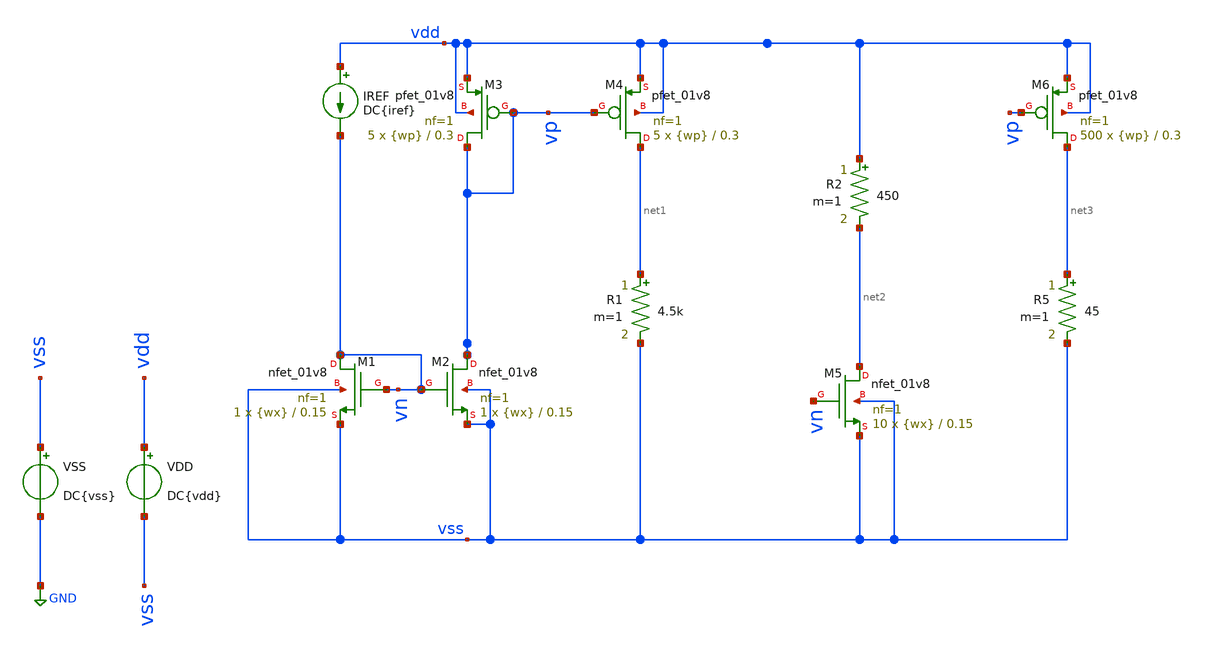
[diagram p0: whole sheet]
** sch_path: tp2/tp2_4.sch
**.subckt tp2_4
XM1 vn vn vss vss sky130_fd_pr__nfet_01v8 L=0.15 W={wx} nf=1 ad='int((nf+1)/2) * W/nf * 0.29' as='int((nf+2)/2) * W/nf * 0.29'
+ pd='2*int((nf+1)/2) * (W/nf + 0.29)' ps='2*int((nf+2)/2) * (W/nf + 0.29)' nrd='0.29 / W' nrs='0.29 / W'
+ sa=0 sb=0 sd=0 mult=1 m=1
IREF vdd vn DC{iref}
VSS vss GND DC{vss}
VDD vdd vss DC{vdd}
XM2 vp vn vss vss sky130_fd_pr__nfet_01v8 L=0.15 W={wx} nf=1 ad='int((nf+1)/2) * W/nf * 0.29' as='int((nf+2)/2) * W/nf * 0.29'
+ pd='2*int((nf+1)/2) * (W/nf + 0.29)' ps='2*int((nf+2)/2) * (W/nf + 0.29)' nrd='0.29 / W' nrs='0.29 / W'
+ sa=0 sb=0 sd=0 mult=1 m=1
XM3 vp vp vdd vdd sky130_fd_pr__pfet_01v8 L=0.3 W={wp} nf=1 ad='int((nf+1)/2) * W/nf * 0.29' as='int((nf+2)/2) * W/nf * 0.29'
+ pd='2*int((nf+1)/2) * (W/nf + 0.29)' ps='2*int((nf+2)/2) * (W/nf + 0.29)' nrd='0.29 / W' nrs='0.29 / W'
+ sa=0 sb=0 sd=0 mult=5 m=5
XM4 net1 vp vdd vdd sky130_fd_pr__pfet_01v8 L=0.3 W={wp} nf=1 ad='int((nf+1)/2) * W/nf * 0.29' as='int((nf+2)/2) * W/nf * 0.29'
+ pd='2*int((nf+1)/2) * (W/nf + 0.29)' ps='2*int((nf+2)/2) * (W/nf + 0.29)' nrd='0.29 / W' nrs='0.29 / W'
+ sa=0 sb=0 sd=0 mult=5 m=5
R1 net1 vss 4.5k m=1
XM5 net2 vn vss vss sky130_fd_pr__nfet_01v8 L=0.15 W={wx} nf=1 ad='int((nf+1)/2) * W/nf * 0.29' as='int((nf+2)/2) * W/nf * 0.29'
+ pd='2*int((nf+1)/2) * (W/nf + 0.29)' ps='2*int((nf+2)/2) * (W/nf + 0.29)' nrd='0.29 / W' nrs='0.29 / W'
+ sa=0 sb=0 sd=0 mult=10 m=10
R2 vdd net2 450 m=1
XM6 net3 vp vdd vdd sky130_fd_pr__pfet_01v8 L=0.3 W={wp} nf=1 ad='int((nf+1)/2) * W/nf * 0.29' as='int((nf+2)/2) * W/nf * 0.29'
+ pd='2*int((nf+1)/2) * (W/nf + 0.29)' ps='2*int((nf+2)/2) * (W/nf + 0.29)' nrd='0.29 / W' nrs='0.29 / W'
+ sa=0 sb=0 sd=0 mult=500 m=500
R5 net3 vss 45 m=1
**** begin user architecture code



* Parameters
.param vdd = 1.98
.param vss = 0.0
.param iref = 200u
.param wp = 97
.param wx = 2.71
.options TEMPS = 27.0

* Models
*.lib ~/skywater/skywater-pdk/libraries/sky130_fd_pr_ngspice/latest/models/corners/sky130.lib TT
.lib /foss/pdks/sky130A/libs.tech/ngspice/sky130.lib.spice tt
* Data to save
.save all  @M.XM1.msky130_fd_pr__nfet_01v8[id]  @M.XM1.msky130_fd_pr__nfet_01v8[gm]  @M.XM1.msky130_fd_pr__nfet_01v8[vds]  @M.XM1.msky130_fd_pr__nfet_01v8[vgs]  @M.XM1.msky130_fd_pr__nfet_01v8[w]  @M.XM1.msky130_fd_pr__nfet_01v8[vth]  @M.XM2.msky130_fd_pr__nfet_01v8[id]  @M.XM2.msky130_fd_pr__nfet_01v8[gm]  @M.XM2.msky130_fd_pr__nfet_01v8[vds]  @M.XM2.msky130_fd_pr__nfet_01v8[vgs]  @M.XM2.msky130_fd_pr__nfet_01v8[w]  @M.XM2.msky130_fd_pr__nfet_01v8[vth]  @M.XM2.msky130_fd_pr__nfet_01v8[vdsat]  @M.XM4.msky130_fd_pr__nfet_01v8[vdsat]  @M.XM7.msky130_fd_pr__nfet_01v8[vdsat]  @M.XM6.msky130_fd_pr__nfet_01v8[vdsat]  @M.XM5.msky130_fd_pr__nfet_01v8[vth]  @M.XM4.msky130_fd_pr__nfet_01v8[vth]  @M.XM1.msky130_fd_pr__nfet_01v8[vth]  @M.XM3.msky130_fd_pr__nfet_01v8[vth]  @M.XM7.msky130_fd_pr__nfet_01v8[vth]  @M.XM6.msky130_fd_pr__nfet_01v8[vth]  @M.XM1.msky130_fd_pr__nfet_01v8[id]  @M.XM2.msky130_fd_pr__nfet_01v8[id]  @M.XM3.msky130_fd_pr__pfet_01v8[id]  @M.XM4.msky130_fd_pr__pfet_01v8[id]  @M.XM5.msky130_fd_pr__nfet_01v8[id]  @M.XM6.msky130_fd_pr__pfet_01v8[id]

* Simulation
.control

  op
  save all
  unset filetype
  write tp2_4.raw

.endc

.end


**** end user architecture code
**.ends
.GLOBAL GND
.end
